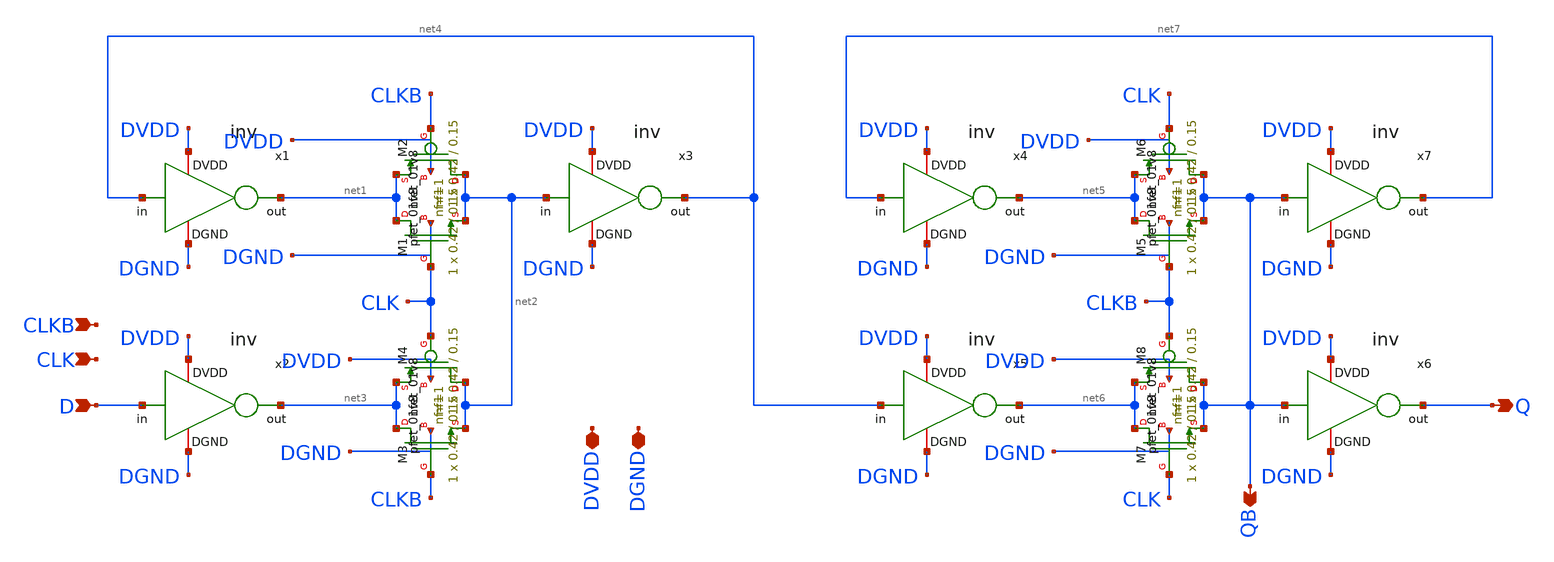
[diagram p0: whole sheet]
** sch_path: tutorial-6/source/pet_dff.sch
**.subckt pet_dff D Q CLK CLKB DVDD DGND QB
*.ipin D
*.opin Q
*.ipin CLK
*.ipin CLKB
*.iopin DVDD
*.iopin DGND
*.opin QB
XM1 net1 CLK net2 DGND sky130_fd_pr__nfet_01v8 L=0.15 W=0.42 nf=1 ad='int((nf+1)/2) * W/nf * 0.29' as='int((nf+2)/2) * W/nf * 0.29'
+ pd='2*int((nf+1)/2) * (W/nf + 0.29)' ps='2*int((nf+2)/2) * (W/nf + 0.29)' nrd='0.29 / W' nrs='0.29 / W'
+ sa=0 sb=0 sd=0 mult=1 m=1
XM2 net2 CLKB net1 DVDD sky130_fd_pr__pfet_01v8 L=0.15 W=0.42 nf=1 ad='int((nf+1)/2) * W/nf * 0.29' as='int((nf+2)/2) * W/nf * 0.29'
+ pd='2*int((nf+1)/2) * (W/nf + 0.29)' ps='2*int((nf+2)/2) * (W/nf + 0.29)' nrd='0.29 / W' nrs='0.29 / W'
+ sa=0 sb=0 sd=0 mult=1 m=1
XM3 net3 CLKB net2 DGND sky130_fd_pr__nfet_01v8 L=0.15 W=0.42 nf=1 ad='int((nf+1)/2) * W/nf * 0.29' as='int((nf+2)/2) * W/nf * 0.29'
+ pd='2*int((nf+1)/2) * (W/nf + 0.29)' ps='2*int((nf+2)/2) * (W/nf + 0.29)' nrd='0.29 / W' nrs='0.29 / W'
+ sa=0 sb=0 sd=0 mult=1 m=1
XM4 net2 CLK net3 DVDD sky130_fd_pr__pfet_01v8 L=0.15 W=0.42 nf=1 ad='int((nf+1)/2) * W/nf * 0.29' as='int((nf+2)/2) * W/nf * 0.29'
+ pd='2*int((nf+1)/2) * (W/nf + 0.29)' ps='2*int((nf+2)/2) * (W/nf + 0.29)' nrd='0.29 / W' nrs='0.29 / W'
+ sa=0 sb=0 sd=0 mult=1 m=1
XM5 net5 CLKB QB DGND sky130_fd_pr__nfet_01v8 L=0.15 W=0.42 nf=1 ad='int((nf+1)/2) * W/nf * 0.29' as='int((nf+2)/2) * W/nf * 0.29'
+ pd='2*int((nf+1)/2) * (W/nf + 0.29)' ps='2*int((nf+2)/2) * (W/nf + 0.29)' nrd='0.29 / W' nrs='0.29 / W'
+ sa=0 sb=0 sd=0 mult=1 m=1
XM6 QB CLK net5 DVDD sky130_fd_pr__pfet_01v8 L=0.15 W=0.42 nf=1 ad='int((nf+1)/2) * W/nf * 0.29' as='int((nf+2)/2) * W/nf * 0.29'
+ pd='2*int((nf+1)/2) * (W/nf + 0.29)' ps='2*int((nf+2)/2) * (W/nf + 0.29)' nrd='0.29 / W' nrs='0.29 / W'
+ sa=0 sb=0 sd=0 mult=1 m=1
XM7 net6 CLK QB DGND sky130_fd_pr__nfet_01v8 L=0.15 W=0.42 nf=1 ad='int((nf+1)/2) * W/nf * 0.29' as='int((nf+2)/2) * W/nf * 0.29'
+ pd='2*int((nf+1)/2) * (W/nf + 0.29)' ps='2*int((nf+2)/2) * (W/nf + 0.29)' nrd='0.29 / W' nrs='0.29 / W'
+ sa=0 sb=0 sd=0 mult=1 m=1
XM8 QB CLKB net6 DVDD sky130_fd_pr__pfet_01v8 L=0.15 W=0.42 nf=1 ad='int((nf+1)/2) * W/nf * 0.29' as='int((nf+2)/2) * W/nf * 0.29'
+ pd='2*int((nf+1)/2) * (W/nf + 0.29)' ps='2*int((nf+2)/2) * (W/nf + 0.29)' nrd='0.29 / W' nrs='0.29 / W'
+ sa=0 sb=0 sd=0 mult=1 m=1
x1 DVDD net4 net1 DGND inv
x2 DVDD D net3 DGND inv
x3 DVDD net2 net4 DGND inv
x4 DVDD net7 net5 DGND inv
x5 DVDD net4 net6 DGND inv
x6 DVDD QB Q DGND inv
x7 DVDD QB net7 DGND inv
**.ends

* expanding   symbol:  inv.sym # of pins=4
** sym_path: tutorial-6/source/inv.sym
** sch_path: tutorial-6/source/inv.sch
.subckt inv DVDD in out DGND
*.iopin DVDD
*.iopin DGND
*.ipin in
*.opin out
XM1 out in DVDD DVDD sky130_fd_pr__pfet_01v8 L=0.15 W=0.84 nf=1 ad='int((nf+1)/2) * W/nf * 0.29' as='int((nf+2)/2) * W/nf * 0.29'
+ pd='2*int((nf+1)/2) * (W/nf + 0.29)' ps='2*int((nf+2)/2) * (W/nf + 0.29)' nrd='0.29 / W' nrs='0.29 / W'
+ sa=0 sb=0 sd=0 mult=1 m=1
XM2 out in DGND DGND sky130_fd_pr__nfet_01v8 L=0.15 W=0.42 nf=1 ad='int((nf+1)/2) * W/nf * 0.29' as='int((nf+2)/2) * W/nf * 0.29'
+ pd='2*int((nf+1)/2) * (W/nf + 0.29)' ps='2*int((nf+2)/2) * (W/nf + 0.29)' nrd='0.29 / W' nrs='0.29 / W'
+ sa=0 sb=0 sd=0 mult=1 m=1
.ends

.end
